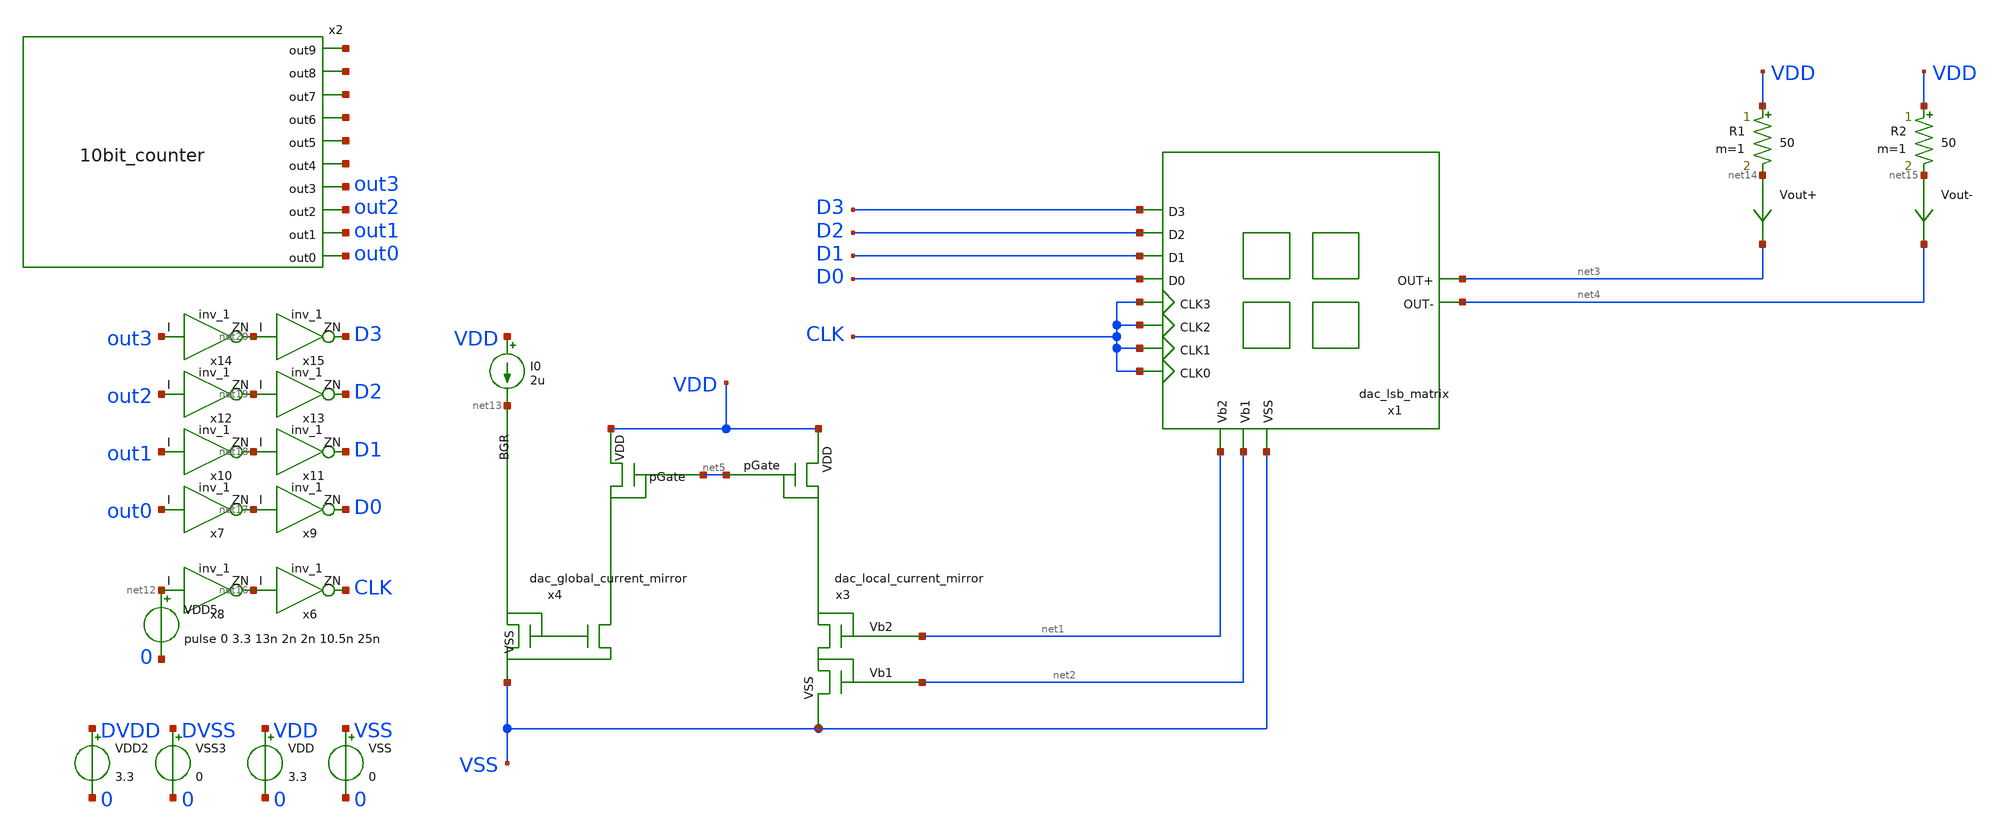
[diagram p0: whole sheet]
** sch_path: DAC/xschem/tb/tb_dac_lsb_matrix.sch
**.subckt tb_dac_lsb_matrix
x2 out0 out1 out2 out3 net6 net7 net8 net9 net10 net11 10bit_counter
VDD VDD 0 3.3
VSS VSS 0 0
VDD2 DVDD 0 3.3
VSS3 DVSS 0 0
VDD5 net12 0 pulse 0 3.3 13n 2n 2n 10.5n 25n
x3 VDD net5 net1 net2 VSS dac_local_current_mirror
x4 VDD net5 net13 VSS dac_global_current_mirror
I0 VDD net13 2u
R1 VDD net14 50 m=1
R2 VDD net15 50 m=1
Vout+ net14 net3 0
.save i(vout+)
Vout- net15 net4 0
.save i(vout-)
x1 D3 D2 D1 D0 CLK CLK CLK CLK net1 net2 VSS net3 net4 DVDD DVSS dac_lsb_matrix
x8 net12 net16 DVDD DVDD DVSS DVSS gf180mcu_fd_sc_mcu7t5v0__inv_1
x6 net16 CLK DVDD DVDD DVSS DVSS gf180mcu_fd_sc_mcu7t5v0__inv_1
x7 out0 net17 DVDD DVDD DVSS DVSS gf180mcu_fd_sc_mcu7t5v0__inv_1
x9 net17 D0 DVDD DVDD DVSS DVSS gf180mcu_fd_sc_mcu7t5v0__inv_1
x10 out1 net18 DVDD DVDD DVSS DVSS gf180mcu_fd_sc_mcu7t5v0__inv_1
x11 net18 D1 DVDD DVDD DVSS DVSS gf180mcu_fd_sc_mcu7t5v0__inv_1
x12 out2 net19 DVDD DVDD DVSS DVSS gf180mcu_fd_sc_mcu7t5v0__inv_1
x13 net19 D2 DVDD DVDD DVSS DVSS gf180mcu_fd_sc_mcu7t5v0__inv_1
x14 out3 net20 DVDD DVDD DVSS DVSS gf180mcu_fd_sc_mcu7t5v0__inv_1
x15 net20 D3 DVDD DVDD DVSS DVSS gf180mcu_fd_sc_mcu7t5v0__inv_1
**** begin user architecture code

.include $::180MCU_MODELS/design.ngspice
.lib $::180MCU_MODELS/sm141064.ngspice typical
.lib $::180MCU_MODELS/sm141064.ngspice res_typical
.lib $::180MCU_MODELS/sm141064.ngspice moscap_typical
.include $::180MCU_STDCELLS/spice/gf180mcu_fd_sc_mcu7t5v0.spice
*.lib $::180MCU_MODELS/sm141064.ngspice res_statistical



.options savecurrents

.control
    tran 1n 400n
    ****plot output currents****
    plot i(Vout+) i(Vout-)
    ****plot input and clock signals****
    plot v(out0)+2*v(out1)+4*v(out2)+8*v(out3) v(clk)
    write tb_dac_lsb.raw
.endc

.save all


**** end user architecture code
**.ends

* expanding   symbol:  10bit_counter.sym # of pins=10
** sym_path: DAC/xschem/10bit_counter.sym
.include /home/junbeom/pico/designs/xschem/10bit_Counter.sp

* expanding   symbol:  dac_local_current_mirror.sym # of pins=5
** sym_path: DAC/xschem/dac_local_current_mirror.sym
** sch_path: DAC/xschem/dac_local_current_mirror.sch
.subckt dac_local_current_mirror VDD pGate Vb2 Vb1 VSS
*.ipin VSS
*.opin Vb2
*.opin Vb1
*.ipin VDD
*.ipin pGate
XM2 Vb2 pGate VDD VDD pfet_03v3 L=1u W=5u nf=5 ad='int((nf+1)/2) * W/nf * 0.18u' as='int((nf+2)/2) * W/nf * 0.18u'
+ pd='2*int((nf+1)/2) * (W/nf + 0.18u)' ps='2*int((nf+2)/2) * (W/nf + 0.18u)' nrd='0.18u / W' nrs='0.18u / W'
+ sa=0 sb=0 sd=0 m=1
XM5 Vb2 Vb2 Vb1 VSS nfet_03v3 L=1u W=4u nf=4 ad='int((nf+1)/2) * W/nf * 0.18u' as='int((nf+2)/2) * W/nf * 0.18u'
+ pd='2*int((nf+1)/2) * (W/nf + 0.18u)' ps='2*int((nf+2)/2) * (W/nf + 0.18u)' nrd='0.18u / W' nrs='0.18u / W'
+ sa=0 sb=0 sd=0 m=1
XM6 Vb1 Vb1 VSS VSS nfet_03v3 L=1u W=4u nf=4 ad='int((nf+1)/2) * W/nf * 0.18u' as='int((nf+2)/2) * W/nf * 0.18u'
+ pd='2*int((nf+1)/2) * (W/nf + 0.18u)' ps='2*int((nf+2)/2) * (W/nf + 0.18u)' nrd='0.18u / W' nrs='0.18u / W'
+ sa=0 sb=0 sd=0 m=1
.ends


* expanding   symbol:  dac_global_current_mirror.sym # of pins=4
** sym_path: DAC/xschem/dac_global_current_mirror.sym
** sch_path: DAC/xschem/dac_global_current_mirror.sch
.subckt dac_global_current_mirror VDD pGate BGR VSS
*.ipin BGR
*.ipin VDD
*.opin pGate
*.ipin VSS
XM1 pGate pGate VDD VDD pfet_03v3 L=1u W=1u nf=1 ad='int((nf+1)/2) * W/nf * 0.18u' as='int((nf+2)/2) * W/nf * 0.18u'
+ pd='2*int((nf+1)/2) * (W/nf + 0.18u)' ps='2*int((nf+2)/2) * (W/nf + 0.18u)' nrd='0.18u / W' nrs='0.18u / W'
+ sa=0 sb=0 sd=0 m=1
XMN1 BGR BGR VSS VSS nfet_03v3 L=4u W=1u nf=4 ad='int((nf+1)/2) * W/nf * 0.18u' as='int((nf+2)/2) * W/nf * 0.18u'
+ pd='2*int((nf+1)/2) * (W/nf + 0.18u)' ps='2*int((nf+2)/2) * (W/nf + 0.18u)' nrd='0.18u / W' nrs='0.18u / W'
+ sa=0 sb=0 sd=0 m=1
XMN2 pGate BGR VSS VSS nfet_03v3 L=4u W=1u nf=4 ad='int((nf+1)/2) * W/nf * 0.18u' as='int((nf+2)/2) * W/nf * 0.18u'
+ pd='2*int((nf+1)/2) * (W/nf + 0.18u)' ps='2*int((nf+2)/2) * (W/nf + 0.18u)' nrd='0.18u / W' nrs='0.18u / W'
+ sa=0 sb=0 sd=0 m=1
.ends


* expanding   symbol:  dac_lsb_matrix.sym # of pins=13
** sym_path: DAC/xschem/dac_lsb_matrix.sym
** sch_path: DAC/xschem/dac_lsb_matrix.sch
.subckt dac_lsb_matrix D3 D2 D1 D0 CLK3 CLK2 CLK1 CLK0 Vb2 Vb1 VSS OUT+ OUT- DVDD DVSS
*.ipin D3
*.ipin D2
*.ipin D1
*.ipin D0
*.ipin CLK3
*.ipin CLK2
*.ipin CLK1
*.ipin CLK0
*.ipin VSS
*.ipin Vb2
*.ipin Vb1
*.opin OUT+
*.opin OUT-
x1 OUT+ OUT- net4 net1 net6 net3 net2 net7 net8 net5 Vb2 Vb1 VSS dac_lsb_analog
x6 D3 CLK3 net1 DVDD DVDD DVSS DVSS gf180mcu_fd_sc_mcu7t5v0__dffq_1
x7 net1 net2 DVDD DVDD DVSS DVSS gf180mcu_fd_sc_mcu7t5v0__inv_1
x4 D2 CLK2 net3 DVDD DVDD DVSS DVSS gf180mcu_fd_sc_mcu7t5v0__dffq_1
x5 net3 net4 DVDD DVDD DVSS DVSS gf180mcu_fd_sc_mcu7t5v0__inv_1
x3 D1 CLK1 net7 DVDD DVDD DVSS DVSS gf180mcu_fd_sc_mcu7t5v0__dffq_1
x8 net7 net6 DVDD DVDD DVSS DVSS gf180mcu_fd_sc_mcu7t5v0__inv_1
x2 D0 CLK0 net5 DVDD DVDD DVSS DVSS gf180mcu_fd_sc_mcu7t5v0__dffq_1
x9 net5 net8 DVDD DVDD DVSS DVSS gf180mcu_fd_sc_mcu7t5v0__inv_1
.ends


* expanding   symbol:  dac_lsb_analog.sym # of pins=13
** sym_path: DAC/xschem/dac_lsb_analog.sym
** sch_path: DAC/xschem/dac_lsb_analog.sch
.subckt dac_lsb_analog OUT+ OUT- Q2- Q3+ Q1- Q2+ Q3- Q1+ Q0- Q0+ Vb2 Vb1 VSS
*.ipin VSS
*.ipin Vb2
*.ipin Vb1
*.ipin Q3-
*.ipin Q3+
*.ipin Q2-
*.ipin Q2+
*.ipin Q1-
*.ipin Q1+
*.ipin Q0-
*.ipin Q0+
*.opin OUT+
*.opin OUT-
XM7 net1 Vb2 net2 VSS nfet_03v3 L=0.5u W=2u nf=2 ad='int((nf+1)/2) * W/nf * 0.18u' as='int((nf+2)/2) * W/nf * 0.18u'
+ pd='2*int((nf+1)/2) * (W/nf + 0.18u)' ps='2*int((nf+2)/2) * (W/nf + 0.18u)' nrd='0.18u / W' nrs='0.18u / W'
+ sa=0 sb=0 sd=0 m=1
XM8 net2 Vb1 VSS VSS nfet_03v3 L=0.5u W=2u nf=1 ad='int((nf+1)/2) * W/nf * 0.18u' as='int((nf+2)/2) * W/nf * 0.18u'
+ pd='2*int((nf+1)/2) * (W/nf + 0.18u)' ps='2*int((nf+2)/2) * (W/nf + 0.18u)' nrd='0.18u / W' nrs='0.18u / W'
+ sa=0 sb=0 sd=0 m=1
XM12 OUT+ Q0+ net1 VSS nfet_03v3 L=0.5u W=1u nf=1 ad='int((nf+1)/2) * W/nf * 0.18u' as='int((nf+2)/2) * W/nf * 0.18u'
+ pd='2*int((nf+1)/2) * (W/nf + 0.18u)' ps='2*int((nf+2)/2) * (W/nf + 0.18u)' nrd='0.18u / W' nrs='0.18u / W'
+ sa=0 sb=0 sd=0 m=1
XM13 OUT- Q0- net1 VSS nfet_03v3 L=0.5u W=1u nf=1 ad='int((nf+1)/2) * W/nf * 0.18u' as='int((nf+2)/2) * W/nf * 0.18u'
+ pd='2*int((nf+1)/2) * (W/nf + 0.18u)' ps='2*int((nf+2)/2) * (W/nf + 0.18u)' nrd='0.18u / W' nrs='0.18u / W'
+ sa=0 sb=0 sd=0 m=1
XM14 net3 Vb2 net4 VSS nfet_03v3 L=0.5u W=4u nf=4 ad='int((nf+1)/2) * W/nf * 0.18u' as='int((nf+2)/2) * W/nf * 0.18u'
+ pd='2*int((nf+1)/2) * (W/nf + 0.18u)' ps='2*int((nf+2)/2) * (W/nf + 0.18u)' nrd='0.18u / W' nrs='0.18u / W'
+ sa=0 sb=0 sd=0 m=1
XM15 net4 Vb1 VSS VSS nfet_03v3 L=0.5u W=4u nf=2 ad='int((nf+1)/2) * W/nf * 0.18u' as='int((nf+2)/2) * W/nf * 0.18u'
+ pd='2*int((nf+1)/2) * (W/nf + 0.18u)' ps='2*int((nf+2)/2) * (W/nf + 0.18u)' nrd='0.18u / W' nrs='0.18u / W'
+ sa=0 sb=0 sd=0 m=1
XM18 OUT+ Q1+ net3 VSS nfet_03v3 L=0.5u W=2u nf=2 ad='int((nf+1)/2) * W/nf * 0.18u' as='int((nf+2)/2) * W/nf * 0.18u'
+ pd='2*int((nf+1)/2) * (W/nf + 0.18u)' ps='2*int((nf+2)/2) * (W/nf + 0.18u)' nrd='0.18u / W' nrs='0.18u / W'
+ sa=0 sb=0 sd=0 m=1
XM19 OUT- Q1- net3 VSS nfet_03v3 L=0.5u W=2u nf=2 ad='int((nf+1)/2) * W/nf * 0.18u' as='int((nf+2)/2) * W/nf * 0.18u'
+ pd='2*int((nf+1)/2) * (W/nf + 0.18u)' ps='2*int((nf+2)/2) * (W/nf + 0.18u)' nrd='0.18u / W' nrs='0.18u / W'
+ sa=0 sb=0 sd=0 m=1
XM20 net5 Vb2 net6 VSS nfet_03v3 L=0.5u W=8u nf=8 ad='int((nf+1)/2) * W/nf * 0.18u' as='int((nf+2)/2) * W/nf * 0.18u'
+ pd='2*int((nf+1)/2) * (W/nf + 0.18u)' ps='2*int((nf+2)/2) * (W/nf + 0.18u)' nrd='0.18u / W' nrs='0.18u / W'
+ sa=0 sb=0 sd=0 m=1
XM21 net6 Vb1 VSS VSS nfet_03v3 L=0.5u W=8u nf=4 ad='int((nf+1)/2) * W/nf * 0.18u' as='int((nf+2)/2) * W/nf * 0.18u'
+ pd='2*int((nf+1)/2) * (W/nf + 0.18u)' ps='2*int((nf+2)/2) * (W/nf + 0.18u)' nrd='0.18u / W' nrs='0.18u / W'
+ sa=0 sb=0 sd=0 m=1
XM24 OUT+ Q2+ net5 VSS nfet_03v3 L=0.5u W=4u nf=4 ad='int((nf+1)/2) * W/nf * 0.18u' as='int((nf+2)/2) * W/nf * 0.18u'
+ pd='2*int((nf+1)/2) * (W/nf + 0.18u)' ps='2*int((nf+2)/2) * (W/nf + 0.18u)' nrd='0.18u / W' nrs='0.18u / W'
+ sa=0 sb=0 sd=0 m=1
XM25 OUT- Q2- net5 VSS nfet_03v3 L=0.5u W=4u nf=4 ad='int((nf+1)/2) * W/nf * 0.18u' as='int((nf+2)/2) * W/nf * 0.18u'
+ pd='2*int((nf+1)/2) * (W/nf + 0.18u)' ps='2*int((nf+2)/2) * (W/nf + 0.18u)' nrd='0.18u / W' nrs='0.18u / W'
+ sa=0 sb=0 sd=0 m=1
XM26 net7 Vb2 net8 VSS nfet_03v3 L=0.5u W=16u nf=16 ad='int((nf+1)/2) * W/nf * 0.18u' as='int((nf+2)/2) * W/nf * 0.18u'
+ pd='2*int((nf+1)/2) * (W/nf + 0.18u)' ps='2*int((nf+2)/2) * (W/nf + 0.18u)' nrd='0.18u / W' nrs='0.18u / W'
+ sa=0 sb=0 sd=0 m=1
XM27 net8 Vb1 VSS VSS nfet_03v3 L=0.5u W=16u nf=8 ad='int((nf+1)/2) * W/nf * 0.18u' as='int((nf+2)/2) * W/nf * 0.18u'
+ pd='2*int((nf+1)/2) * (W/nf + 0.18u)' ps='2*int((nf+2)/2) * (W/nf + 0.18u)' nrd='0.18u / W' nrs='0.18u / W'
+ sa=0 sb=0 sd=0 m=1
XM30 OUT+ Q3+ net7 VSS nfet_03v3 L=0.5u W=8u nf=8 ad='int((nf+1)/2) * W/nf * 0.18u' as='int((nf+2)/2) * W/nf * 0.18u'
+ pd='2*int((nf+1)/2) * (W/nf + 0.18u)' ps='2*int((nf+2)/2) * (W/nf + 0.18u)' nrd='0.18u / W' nrs='0.18u / W'
+ sa=0 sb=0 sd=0 m=1
XM31 OUT- Q3- net7 VSS nfet_03v3 L=0.5u W=8u nf=8 ad='int((nf+1)/2) * W/nf * 0.18u' as='int((nf+2)/2) * W/nf * 0.18u'
+ pd='2*int((nf+1)/2) * (W/nf + 0.18u)' ps='2*int((nf+2)/2) * (W/nf + 0.18u)' nrd='0.18u / W' nrs='0.18u / W'
+ sa=0 sb=0 sd=0 m=1
.ends

.end
